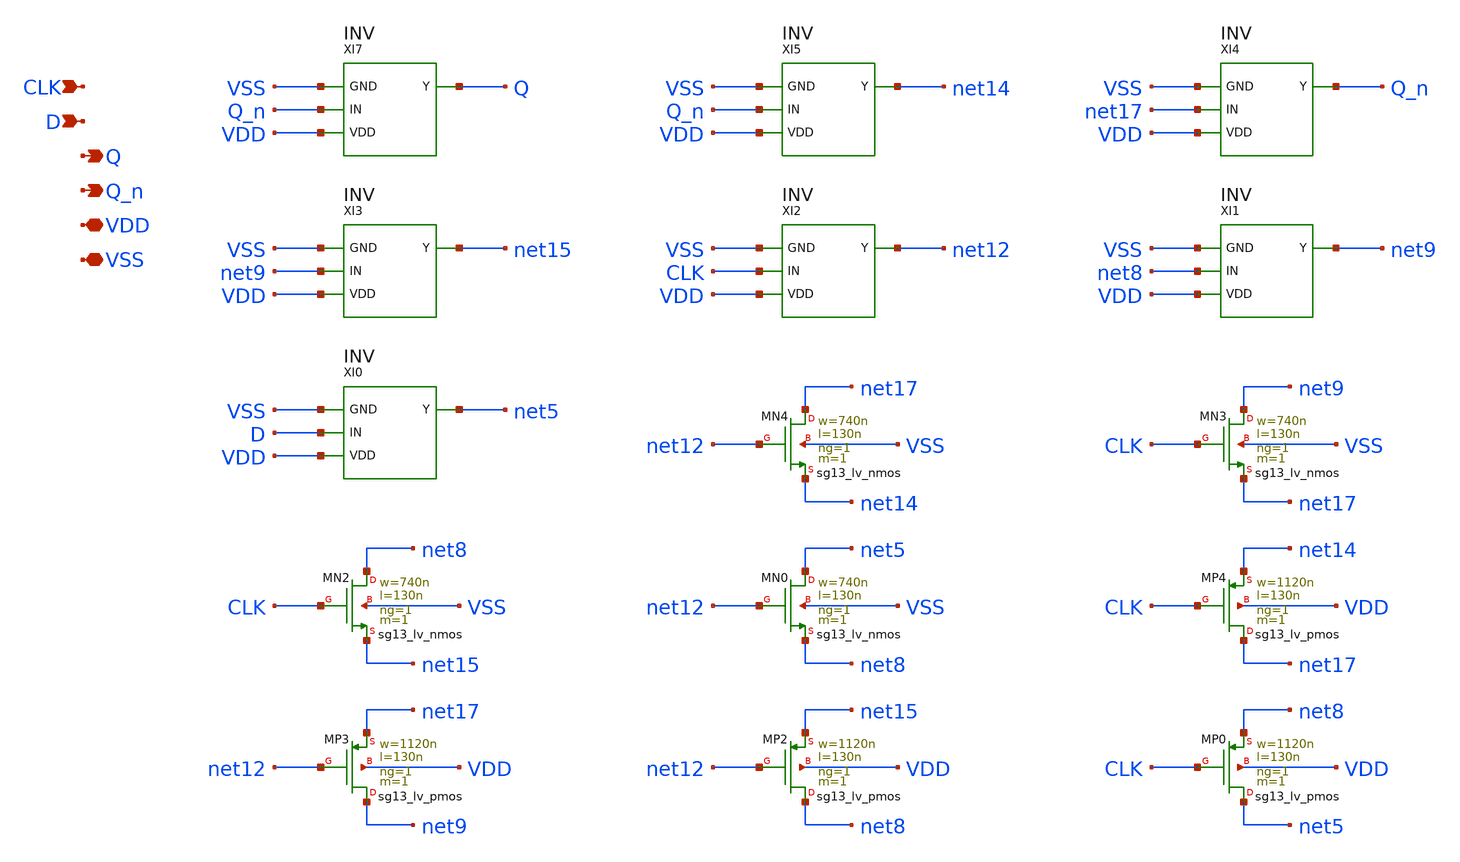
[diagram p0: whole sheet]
** sch_path: SoC6169-main/schematic/xschem/flip_flop.sch
* Copyright 2026 USFQ CAM team
* Licensed under the Apache License, Version 2.0 (the "License");
* you may not use this file except in compliance with the License.
* You may obtain a copy of the License at
* https://www.apache.org/licenses/LICENSE-2.0
* Unless required by applicable law or agreed to in writing, software
* distributed under the License is distributed on an "AS IS" BASIS,
* WITHOUT WARRANTIES OR CONDITIONS OF ANY KIND, either express or implied.
* See the License for the specific language governing permissions and
* limitations under the License.
**.subckt flip_flop CLK D Q Q_n VDD VSS
*.ipin CLK
*.ipin D
*.opin Q
*.opin Q_n
*.iopin VDD
*.iopin VSS
XI7 VSS Q_n VDD Q INV
XI5 VSS Q_n VDD net14 INV
XI4 VSS net17 VDD Q_n INV
XI3 VSS net9 VDD net15 INV
XI2 VSS CLK VDD net12 INV
XI1 VSS net8 VDD net9 INV
XI0 VSS D VDD net5 INV
XMN4 net17 net12 net14 VSS sg13_lv_nmos w=740n l=130n ng=1 m=1 mm_ok=1
XMN3 net9 CLK net17 VSS sg13_lv_nmos w=740n l=130n ng=1 m=1 mm_ok=1
XMN2 net8 CLK net15 VSS sg13_lv_nmos w=740n l=130n ng=1 m=1 mm_ok=1
XMN0 net5 net12 net8 VSS sg13_lv_nmos w=740n l=130n ng=1 m=1 mm_ok=1
XMP4 net17 CLK net14 VDD sg13_lv_pmos w=1120n l=130n ng=1 m=1 mm_ok=1
XMP3 net9 net12 net17 VDD sg13_lv_pmos w=1120n l=130n ng=1 m=1 mm_ok=1
XMP2 net8 net12 net15 VDD sg13_lv_pmos w=1120n l=130n ng=1 m=1 mm_ok=1
XMP0 net5 CLK net8 VDD sg13_lv_pmos w=1120n l=130n ng=1 m=1 mm_ok=1
**.ends

* expanding   symbol:  INV.sym # of pins=4
** sym_path: SoC6169-main/schematic/xschem/INV.sym
** sch_path: SoC6169-main/schematic/xschem/INV.sch
.subckt INV GND IN VDD Y
*.iopin GND
*.ipin IN
*.iopin VDD
*.opin Y
XMN0 Y IN GND GND sg13_lv_nmos w=200n l=130n ng=1 m=1 mm_ok=1
XMP0 Y IN VDD VDD sg13_lv_pmos w=400n l=130n ng=1 m=1 mm_ok=1
.ends

.end
